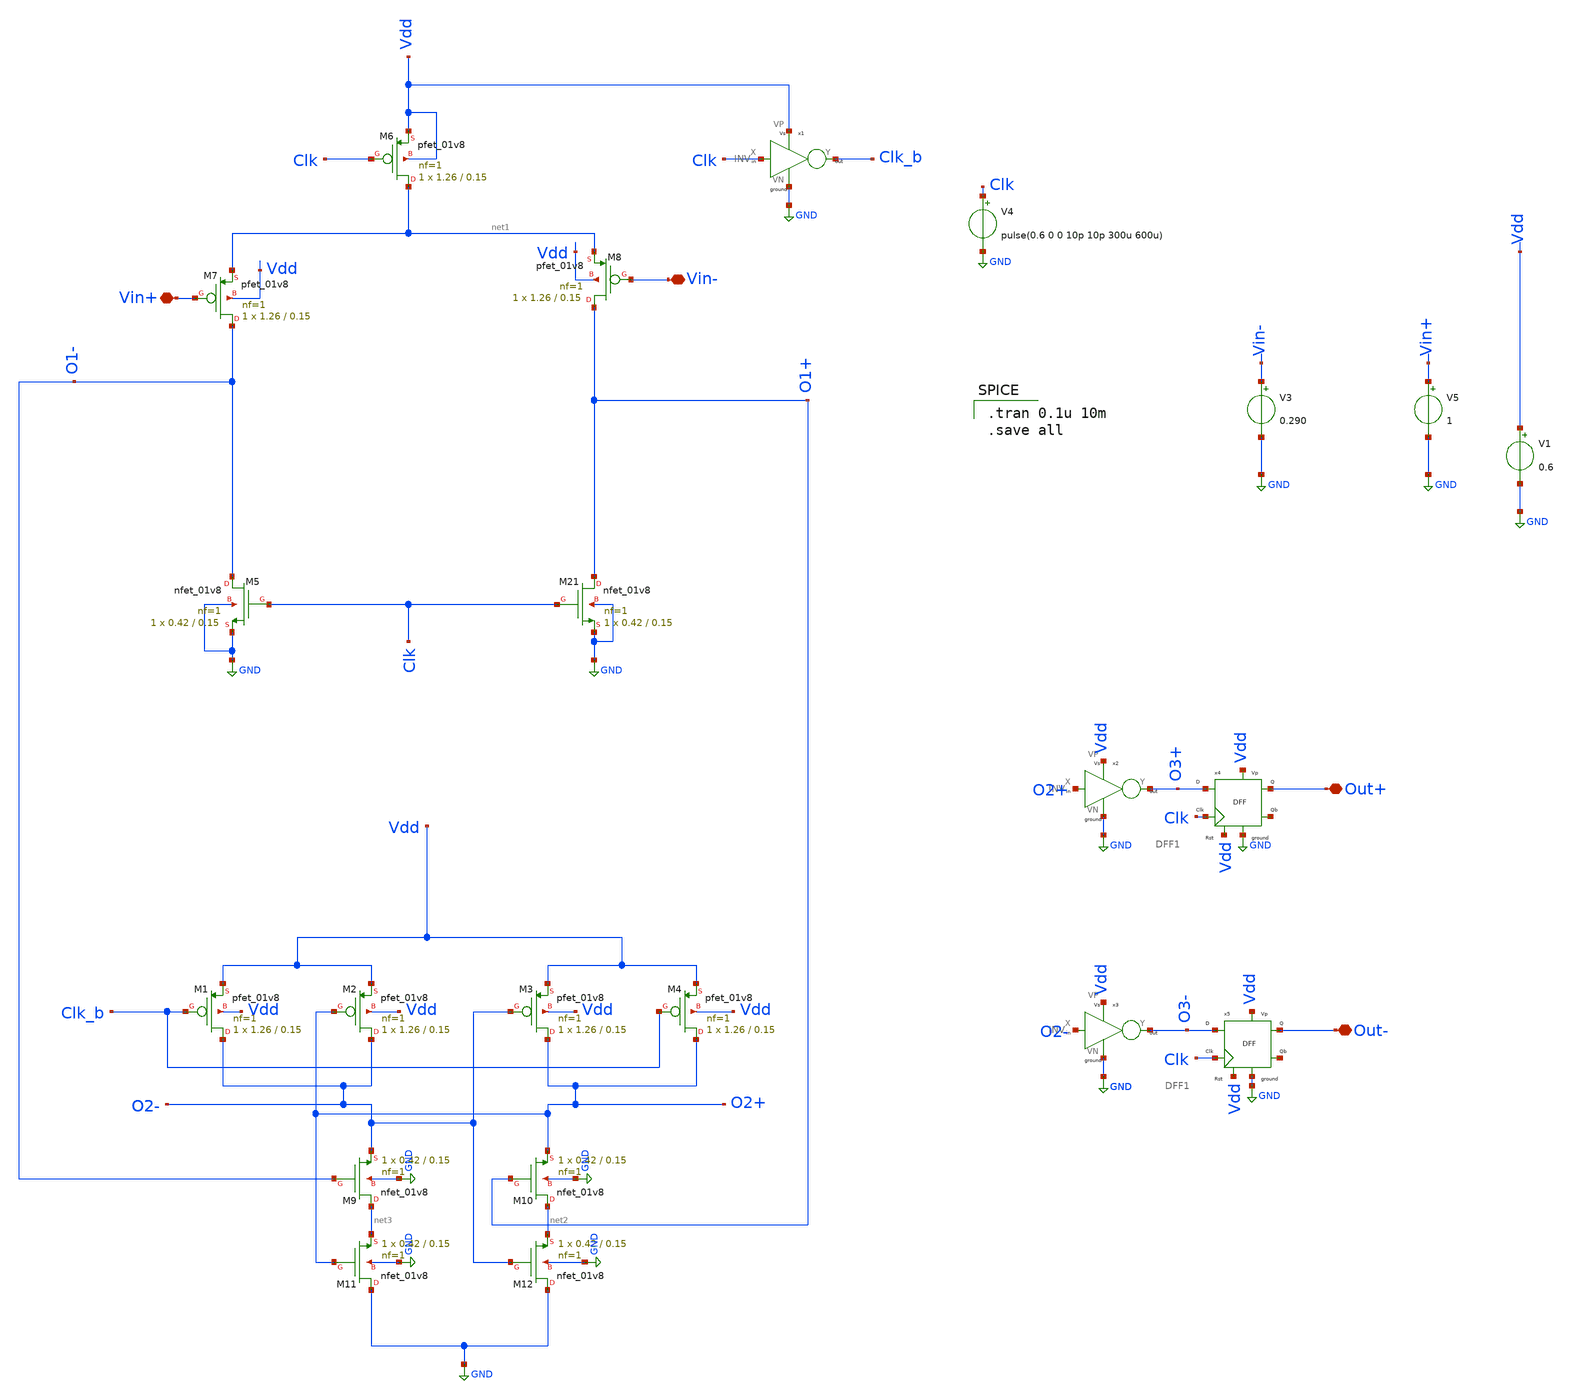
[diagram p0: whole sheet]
** sch_path: Blocks/Conv_comparator/testckt.sch
**.subckt testckt Vin+ Vin- Out+ Out-
*.iopin Vin+
*.iopin Vin-
*.iopin Out+
*.iopin Out-
XM6 net1 Clk Vdd Vdd sky130_fd_pr__pfet_01v8 L=0.15 W=1.26 nf=1 ad='int((nf+1)/2) * W/nf * 0.29' as='int((nf+2)/2) * W/nf * 0.29'
+ pd='2*int((nf+1)/2) * (W/nf + 0.29)' ps='2*int((nf+2)/2) * (W/nf + 0.29)' nrd='0.29 / W' nrs='0.29 / W'
+ sa=0 sb=0 sd=0 mult=1 m=1
XM7 O1- Vin+ net1 Vdd sky130_fd_pr__pfet_01v8 L=0.15 W=1.26 nf=1 ad='int((nf+1)/2) * W/nf * 0.29' as='int((nf+2)/2) * W/nf * 0.29'
+ pd='2*int((nf+1)/2) * (W/nf + 0.29)' ps='2*int((nf+2)/2) * (W/nf + 0.29)' nrd='0.29 / W' nrs='0.29 / W'
+ sa=0 sb=0 sd=0 mult=1 m=1
XM8 O1+ Vin- net1 Vdd sky130_fd_pr__pfet_01v8 L=0.15 W=1.26 nf=1 ad='int((nf+1)/2) * W/nf * 0.29' as='int((nf+2)/2) * W/nf * 0.29'
+ pd='2*int((nf+1)/2) * (W/nf + 0.29)' ps='2*int((nf+2)/2) * (W/nf + 0.29)' nrd='0.29 / W' nrs='0.29 / W'
+ sa=0 sb=0 sd=0 mult=1 m=1
XM5 O1- Clk GND GND sky130_fd_pr__nfet_01v8 L=0.15 W=0.42 nf=1 ad='int((nf+1)/2) * W/nf * 0.29' as='int((nf+2)/2) * W/nf * 0.29'
+ pd='2*int((nf+1)/2) * (W/nf + 0.29)' ps='2*int((nf+2)/2) * (W/nf + 0.29)' nrd='0.29 / W' nrs='0.29 / W'
+ sa=0 sb=0 sd=0 mult=1 m=1
XM21 O1+ Clk GND GND sky130_fd_pr__nfet_01v8 L=0.15 W=0.42 nf=1 ad='int((nf+1)/2) * W/nf * 0.29' as='int((nf+2)/2) * W/nf * 0.29'
+ pd='2*int((nf+1)/2) * (W/nf + 0.29)' ps='2*int((nf+2)/2) * (W/nf + 0.29)' nrd='0.29 / W' nrs='0.29 / W'
+ sa=0 sb=0 sd=0 mult=1 m=1
XM1 O2- Clk_b Vdd Vdd sky130_fd_pr__pfet_01v8 L=0.15 W=1.26 nf=1 ad='int((nf+1)/2) * W/nf * 0.29' as='int((nf+2)/2) * W/nf * 0.29'
+ pd='2*int((nf+1)/2) * (W/nf + 0.29)' ps='2*int((nf+2)/2) * (W/nf + 0.29)' nrd='0.29 / W' nrs='0.29 / W'
+ sa=0 sb=0 sd=0 mult=1 m=1
XM2 O2- O2+ Vdd Vdd sky130_fd_pr__pfet_01v8 L=0.15 W=1.26 nf=1 ad='int((nf+1)/2) * W/nf * 0.29' as='int((nf+2)/2) * W/nf * 0.29'
+ pd='2*int((nf+1)/2) * (W/nf + 0.29)' ps='2*int((nf+2)/2) * (W/nf + 0.29)' nrd='0.29 / W' nrs='0.29 / W'
+ sa=0 sb=0 sd=0 mult=1 m=1
XM3 O2+ O2- Vdd Vdd sky130_fd_pr__pfet_01v8 L=0.15 W=1.26 nf=1 ad='int((nf+1)/2) * W/nf * 0.29' as='int((nf+2)/2) * W/nf * 0.29'
+ pd='2*int((nf+1)/2) * (W/nf + 0.29)' ps='2*int((nf+2)/2) * (W/nf + 0.29)' nrd='0.29 / W' nrs='0.29 / W'
+ sa=0 sb=0 sd=0 mult=1 m=1
XM4 O2+ Clk_b Vdd Vdd sky130_fd_pr__pfet_01v8 L=0.15 W=1.26 nf=1 ad='int((nf+1)/2) * W/nf * 0.29' as='int((nf+2)/2) * W/nf * 0.29'
+ pd='2*int((nf+1)/2) * (W/nf + 0.29)' ps='2*int((nf+2)/2) * (W/nf + 0.29)' nrd='0.29 / W' nrs='0.29 / W'
+ sa=0 sb=0 sd=0 mult=1 m=1
XM9 net3 O1- O2- GND sky130_fd_pr__nfet_01v8 L=0.15 W=0.42 nf=1 ad='int((nf+1)/2) * W/nf * 0.29' as='int((nf+2)/2) * W/nf * 0.29'
+ pd='2*int((nf+1)/2) * (W/nf + 0.29)' ps='2*int((nf+2)/2) * (W/nf + 0.29)' nrd='0.29 / W' nrs='0.29 / W'
+ sa=0 sb=0 sd=0 mult=1 m=1
XM10 net2 O1+ O2+ GND sky130_fd_pr__nfet_01v8 L=0.15 W=0.42 nf=1 ad='int((nf+1)/2) * W/nf * 0.29' as='int((nf+2)/2) * W/nf * 0.29'
+ pd='2*int((nf+1)/2) * (W/nf + 0.29)' ps='2*int((nf+2)/2) * (W/nf + 0.29)' nrd='0.29 / W' nrs='0.29 / W'
+ sa=0 sb=0 sd=0 mult=1 m=1
XM11 GND O2+ net3 GND sky130_fd_pr__nfet_01v8 L=0.15 W=0.42 nf=1 ad='int((nf+1)/2) * W/nf * 0.29' as='int((nf+2)/2) * W/nf * 0.29'
+ pd='2*int((nf+1)/2) * (W/nf + 0.29)' ps='2*int((nf+2)/2) * (W/nf + 0.29)' nrd='0.29 / W' nrs='0.29 / W'
+ sa=0 sb=0 sd=0 mult=1 m=1
XM12 GND O2- net2 GND sky130_fd_pr__nfet_01v8 L=0.15 W=0.42 nf=1 ad='int((nf+1)/2) * W/nf * 0.29' as='int((nf+2)/2) * W/nf * 0.29'
+ pd='2*int((nf+1)/2) * (W/nf + 0.29)' ps='2*int((nf+2)/2) * (W/nf + 0.29)' nrd='0.29 / W' nrs='0.29 / W'
+ sa=0 sb=0 sd=0 mult=1 m=1
V3 Vin- GND 0.290
V5 Vin+ GND 1
V1 Vdd GND 0.6
V4 Clk GND pulse(0.6 0 0 10p 10p 300u 600u)
x1 Clk Clk_b Vdd GND INV
x2 O2+ O3+ Vdd GND INV
x3 O2- O3- Vdd GND INV
x4 O3+ Clk Vdd GND Vdd Out+ net4 DFF1
x5 O3- Clk Vdd GND Vdd Out- net5 DFF1
**** begin user architecture code

** opencircuitdesign pdks install
.lib $::SKYWATER_MODELS/sky130.lib.spice tt



.tran 0.1u 10m
.save all

**** end user architecture code
**.ends

* expanding   symbol:  pico_chipathon/component/INV/INV.sym # of pins=4
** sym_path: component/INV/INV.sym
** sch_path: component/INV/INV.sch
.subckt INV X Y VP VN
*.ipin X
*.opin Y
*.iopin VN
*.iopin VP
XM1 Y X VN VN sky130_fd_pr__nfet_01v8 L=0.15 W=0.42 nf=1 ad='int((nf+1)/2) * W/nf * 0.29' as='int((nf+2)/2) * W/nf * 0.29'
+ pd='2*int((nf+1)/2) * (W/nf + 0.29)' ps='2*int((nf+2)/2) * (W/nf + 0.29)' nrd='0.29 / W' nrs='0.29 / W'
+ sa=0 sb=0 sd=0 mult=1 m=1
XM2 Y X VP VP sky130_fd_pr__pfet_01v8 L=0.15 W=1.26 nf=1 ad='int((nf+1)/2) * W/nf * 0.29' as='int((nf+2)/2) * W/nf * 0.29'
+ pd='2*int((nf+1)/2) * (W/nf + 0.29)' ps='2*int((nf+2)/2) * (W/nf + 0.29)' nrd='0.29 / W' nrs='0.29 / W'
+ sa=0 sb=0 sd=0 mult=1 m=1
.ends


* expanding   symbol:  pico_chipathon/component/FlipFlops/DFF1.sym # of pins=7
** sym_path: component/FlipFlops/DFF1.sym
** sch_path: component/FlipFlops/DFF1.sch
.subckt DFF1 D Clk RST VN VP Q Qb
*.opin Q
*.iopin VN
*.iopin VP
*.ipin Clk
*.ipin D
*.ipin RST
*.opin Qb
x7 net2 net4 net3 VP VN NAND
x8 net3 Clk RST VP VN net2 NAND3
x6 Q net1 RST VP VN Qb NAND3
x4 net2 Clk net4 VP VN net1 NAND3
x5 net1 D RST VP VN net4 NAND3
x1 Qb net2 Q VP VN NAND
.ends


* expanding   symbol:  component/NAND2/NAND.sym # of pins=5
** sym_path: component/NAND2/NAND.sym
** sch_path: component/NAND2/NAND.sch
.subckt NAND B A Y VP VN
*.iopin VP
*.ipin A
*.ipin B
*.opin Y
*.iopin VN
XM1 Y A VP VP sky130_fd_pr__pfet_01v8 L=0.15 W=1.26 nf=1 ad='int((nf+1)/2) * W/nf * 0.29' as='int((nf+2)/2) * W/nf * 0.29'
+ pd='2*int((nf+1)/2) * (W/nf + 0.29)' ps='2*int((nf+2)/2) * (W/nf + 0.29)' nrd='0.29 / W' nrs='0.29 / W'
+ sa=0 sb=0 sd=0 mult=1 m=1
XM2 Y B VP VP sky130_fd_pr__pfet_01v8 L=0.15 W=1.26 nf=1 ad='int((nf+1)/2) * W/nf * 0.29' as='int((nf+2)/2) * W/nf * 0.29'
+ pd='2*int((nf+1)/2) * (W/nf + 0.29)' ps='2*int((nf+2)/2) * (W/nf + 0.29)' nrd='0.29 / W' nrs='0.29 / W'
+ sa=0 sb=0 sd=0 mult=1 m=1
XM3 Y A net1 net1 sky130_fd_pr__nfet_01v8 L=0.15 W=0.84 nf=1 ad='int((nf+1)/2) * W/nf * 0.29' as='int((nf+2)/2) * W/nf * 0.29'
+ pd='2*int((nf+1)/2) * (W/nf + 0.29)' ps='2*int((nf+2)/2) * (W/nf + 0.29)' nrd='0.29 / W' nrs='0.29 / W'
+ sa=0 sb=0 sd=0 mult=1 m=1
XM4 net1 B VN VN sky130_fd_pr__nfet_01v8 L=0.15 W=0.84 nf=1 ad='int((nf+1)/2) * W/nf * 0.29' as='int((nf+2)/2) * W/nf * 0.29'
+ pd='2*int((nf+1)/2) * (W/nf + 0.29)' ps='2*int((nf+2)/2) * (W/nf + 0.29)' nrd='0.29 / W' nrs='0.29 / W'
+ sa=0 sb=0 sd=0 mult=1 m=1
.ends


* expanding   symbol:  component/NAND3/NAND3.sym # of pins=6
** sym_path: component/NAND3/NAND3.sym
** sch_path: component/NAND3/NAND3.sch
.subckt NAND3 A B C VP VN Y
*.iopin VP
*.iopin VN
*.ipin A
*.ipin B
*.ipin C
*.opin Y
XM1 Y A net1 VN sky130_fd_pr__nfet_01v8 L=0.15 W=1.26 nf=1 ad='int((nf+1)/2) * W/nf * 0.29' as='int((nf+2)/2) * W/nf * 0.29'
+ pd='2*int((nf+1)/2) * (W/nf + 0.29)' ps='2*int((nf+2)/2) * (W/nf + 0.29)' nrd='0.29 / W' nrs='0.29 / W'
+ sa=0 sb=0 sd=0 mult=1 m=1
XM2 net1 B net2 VN sky130_fd_pr__nfet_01v8 L=0.15 W=1.26 nf=1 ad='int((nf+1)/2) * W/nf * 0.29' as='int((nf+2)/2) * W/nf * 0.29'
+ pd='2*int((nf+1)/2) * (W/nf + 0.29)' ps='2*int((nf+2)/2) * (W/nf + 0.29)' nrd='0.29 / W' nrs='0.29 / W'
+ sa=0 sb=0 sd=0 mult=1 m=1
XM3 net2 C VN VN sky130_fd_pr__nfet_01v8 L=0.15 W=1.26 nf=1 ad='int((nf+1)/2) * W/nf * 0.29' as='int((nf+2)/2) * W/nf * 0.29'
+ pd='2*int((nf+1)/2) * (W/nf + 0.29)' ps='2*int((nf+2)/2) * (W/nf + 0.29)' nrd='0.29 / W' nrs='0.29 / W'
+ sa=0 sb=0 sd=0 mult=1 m=1
XM4 Y A VP VP sky130_fd_pr__pfet_01v8 L=0.15 W=1.26 nf=1 ad='int((nf+1)/2) * W/nf * 0.29' as='int((nf+2)/2) * W/nf * 0.29'
+ pd='2*int((nf+1)/2) * (W/nf + 0.29)' ps='2*int((nf+2)/2) * (W/nf + 0.29)' nrd='0.29 / W' nrs='0.29 / W'
+ sa=0 sb=0 sd=0 mult=1 m=1
XM5 Y B VP VP sky130_fd_pr__pfet_01v8 L=0.15 W=1.26 nf=1 ad='int((nf+1)/2) * W/nf * 0.29' as='int((nf+2)/2) * W/nf * 0.29'
+ pd='2*int((nf+1)/2) * (W/nf + 0.29)' ps='2*int((nf+2)/2) * (W/nf + 0.29)' nrd='0.29 / W' nrs='0.29 / W'
+ sa=0 sb=0 sd=0 mult=1 m=1
XM6 Y C VP VP sky130_fd_pr__pfet_01v8 L=0.15 W=1.26 nf=1 ad='int((nf+1)/2) * W/nf * 0.29' as='int((nf+2)/2) * W/nf * 0.29'
+ pd='2*int((nf+1)/2) * (W/nf + 0.29)' ps='2*int((nf+2)/2) * (W/nf + 0.29)' nrd='0.29 / W' nrs='0.29 / W'
+ sa=0 sb=0 sd=0 mult=1 m=1
.ends

.GLOBAL GND
.end
